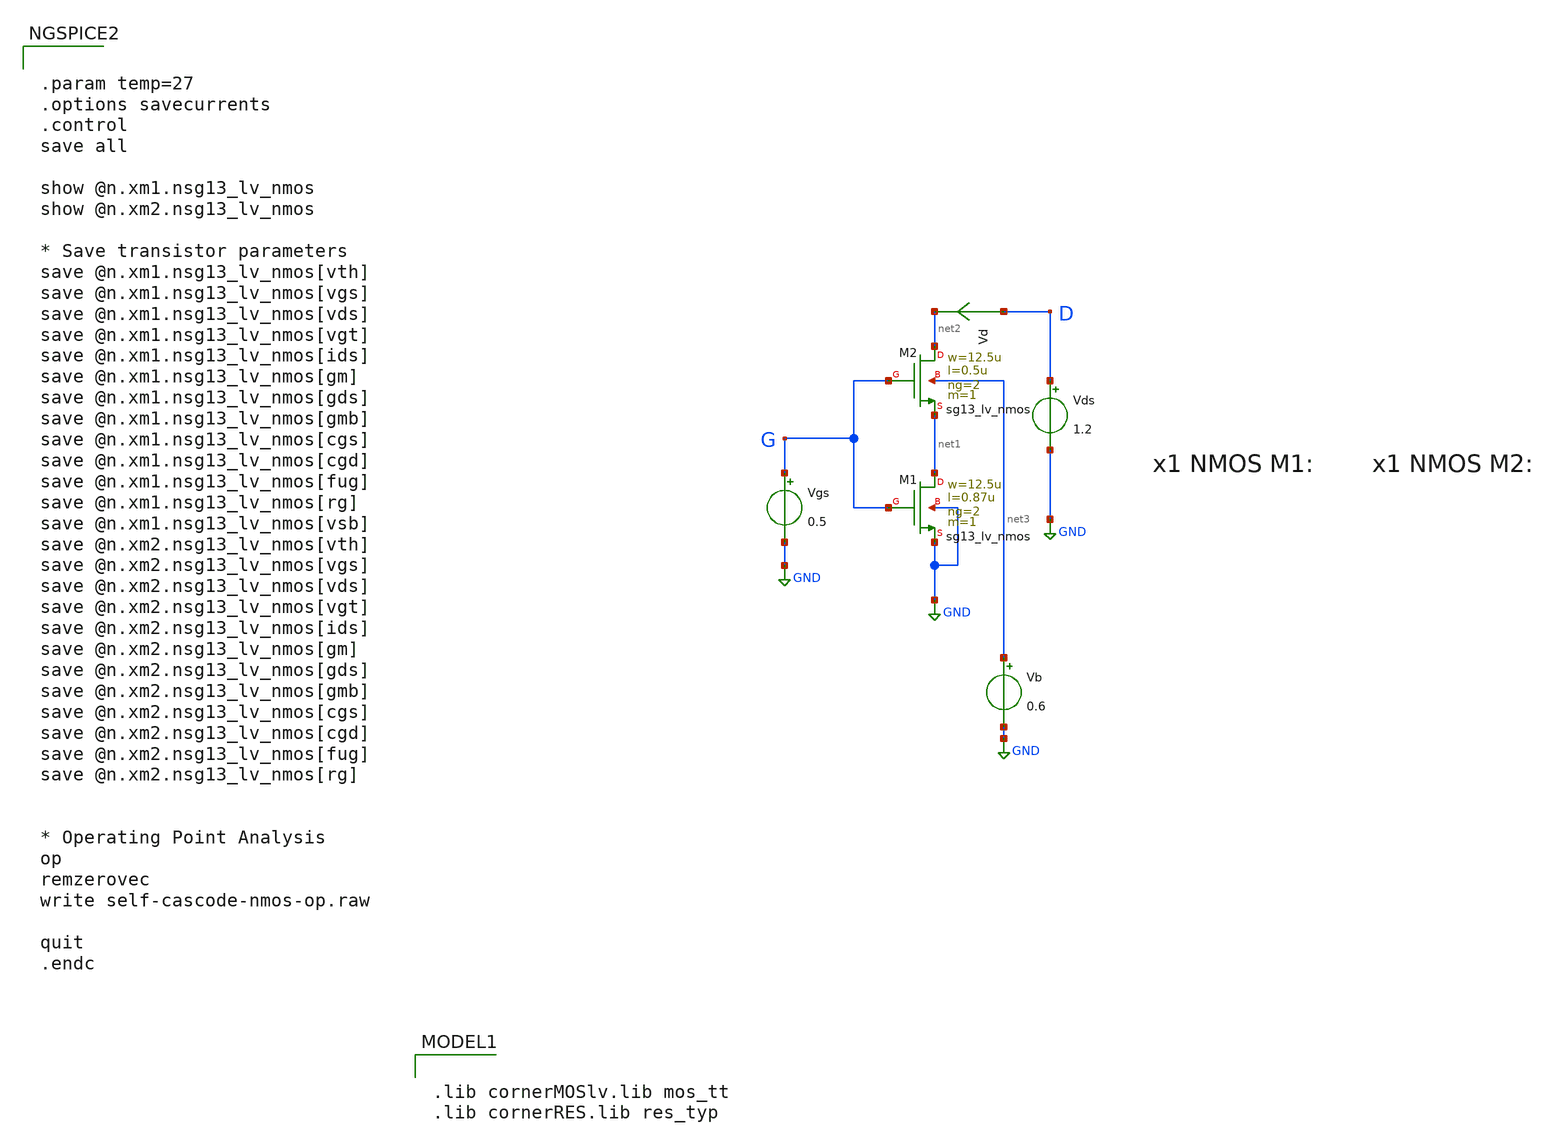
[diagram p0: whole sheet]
** sch_path: xschem/self-cascode-nmos-op.sch
**.subckt self-cascode-nmos-op
Vgs G GND 0.5
Vds D GND 1.2
Vd D net2 0
.save i(vd)
XM1 net1 G GND GND sg13_lv_nmos w=12.5u l=0.87u ng=2 m=1 mm_ok=1
XM2 net2 G net1 net3 sg13_lv_nmos w=12.5u l=0.5u ng=2 m=1 mm_ok=1
Vb net3 GND 0.6
**** begin user architecture code

.lib cornerMOSlv.lib mos_tt
.lib cornerRES.lib res_typ



.param temp=27
.options savecurrents
.control
save all

show @n.xm1.nsg13_lv_nmos
show @n.xm2.nsg13_lv_nmos

* Save transistor parameters
save @n.xm1.nsg13_lv_nmos[vth]
save @n.xm1.nsg13_lv_nmos[vgs]
save @n.xm1.nsg13_lv_nmos[vds]
save @n.xm1.nsg13_lv_nmos[vgt]
save @n.xm1.nsg13_lv_nmos[ids]
save @n.xm1.nsg13_lv_nmos[gm]
save @n.xm1.nsg13_lv_nmos[gds]
save @n.xm1.nsg13_lv_nmos[gmb]
save @n.xm1.nsg13_lv_nmos[cgs]
save @n.xm1.nsg13_lv_nmos[cgd]
save @n.xm1.nsg13_lv_nmos[fug]
save @n.xm1.nsg13_lv_nmos[rg]
save @n.xm1.nsg13_lv_nmos[vsb]
save @n.xm2.nsg13_lv_nmos[vth]
save @n.xm2.nsg13_lv_nmos[vgs]
save @n.xm2.nsg13_lv_nmos[vds]
save @n.xm2.nsg13_lv_nmos[vgt]
save @n.xm2.nsg13_lv_nmos[ids]
save @n.xm2.nsg13_lv_nmos[gm]
save @n.xm2.nsg13_lv_nmos[gds]
save @n.xm2.nsg13_lv_nmos[gmb]
save @n.xm2.nsg13_lv_nmos[cgs]
save @n.xm2.nsg13_lv_nmos[cgd]
save @n.xm2.nsg13_lv_nmos[fug]
save @n.xm2.nsg13_lv_nmos[rg]


* Operating Point Analysis
op
remzerovec
write self-cascode-nmos-op.raw

quit
.endc

**** end user architecture code
**.ends
.GLOBAL GND
.end
